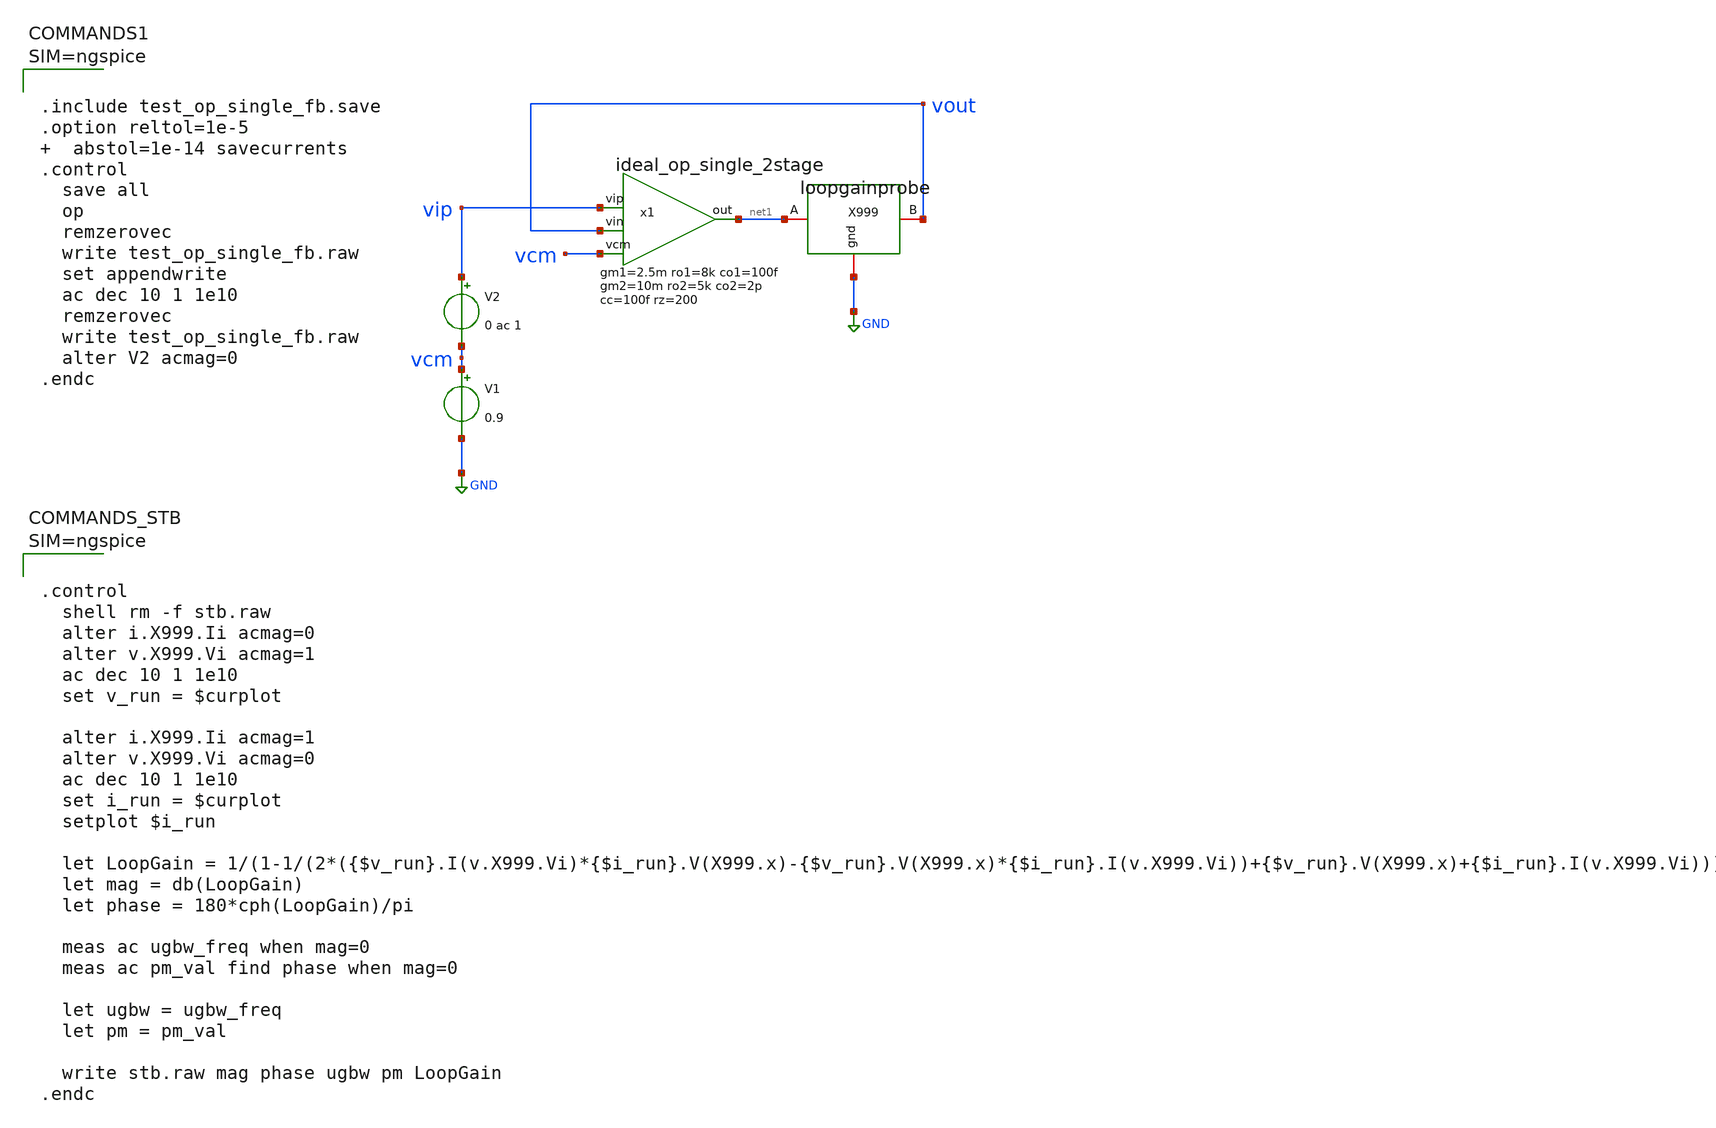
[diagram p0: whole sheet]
** sch_path: test_op_single_fb.sch
**.subckt test_op_single_fb
V1 vcm GND 0.9
V2 vip vcm 0 ac 1
x1 net1 vip vout vcm ideal_op_single_2stage gm1=2.5m ro1=8k co1=100f gm2=10m ro2=5k co2=2p cc=100f
+ rz=200
X999 net1 vout GND loopgainprobe
**** begin user architecture code



.include test_op_single_fb.save
.option reltol=1e-5   abstol=1e-14 savecurrents
.control
  save all
  op
  remzerovec
  write test_op_single_fb.raw
  set appendwrite
  ac dec 10 1 1e10
  remzerovec
  write test_op_single_fb.raw
  alter V2 acmag=0
.endc






.control
  shell rm -f stb.raw
  alter i.X999.Ii acmag=0
  alter v.X999.Vi acmag=1
  ac dec 10 1 1e10
  set v_run = $curplot

  alter i.X999.Ii acmag=1
  alter v.X999.Vi acmag=0
  ac dec 10 1 1e10
  set i_run = $curplot
  setplot $i_run

  let LoopGain = 1/(1-1/(2*({$v_run}.I(v.X999.Vi)*{$i_run}.V(X999.x)-{$v_run}.V(X999.x)*{$i_run}.I(v.X999.Vi))+{$v_run}.V(X999.x)+{$i_run}.I(v.X999.Vi)))
  let mag = db(LoopGain)
  let phase = 180*cph(LoopGain)/pi

  meas ac ugbw_freq when mag=0
  meas ac pm_val find phase when mag=0

  let ugbw = ugbw_freq
  let pm = pm_val

  write stb.raw mag phase ugbw pm LoopGain
.endc



**** end user architecture code
**.ends

* expanding   symbol:  /home/tester/proj/modules/ideal_op_single_2stage.sym # of pins=4
** sym_path: modules/ideal_op_single_2stage.sym
** sch_path: modules/ideal_op_single_2stage.sch
.subckt ideal_op_single_2stage out vip vin vcm  gm1=5m ro1=20k co1=100f gm2=10m ro2=5k co2=2p
+ cc=100f rz=200
*.ipin vip
*.ipin vin
*.opin out
*.ipin vcm
G1 net1 vcm vip vin {gm1}
R1 net1 vcm {ro1} m=1
C1 net1 vcm {co1} m=1
G3 out vcm net1 vcm {gm2}
R3 out vcm {ro2} m=1
C3 out vcm {co2} m=1
R5 net1 net2 {rz} m=1
C5 net2 out {cc} m=1
.ends


* expanding   symbol:  /home/tester/proj/modules/loopgainprobe.sym # of pins=3
** sym_path: modules/loopgainprobe.sym
** sch_path: modules/loopgainprobe.sch
.subckt loopgainprobe A B gnd
*.iopin gnd
*.iopin A
*.iopin B
Ii gnd x DC 0 AC 0
Vi x A DC 0 AC 0
Vnodebuffer B x 0
.ends

.GLOBAL GND
.end
